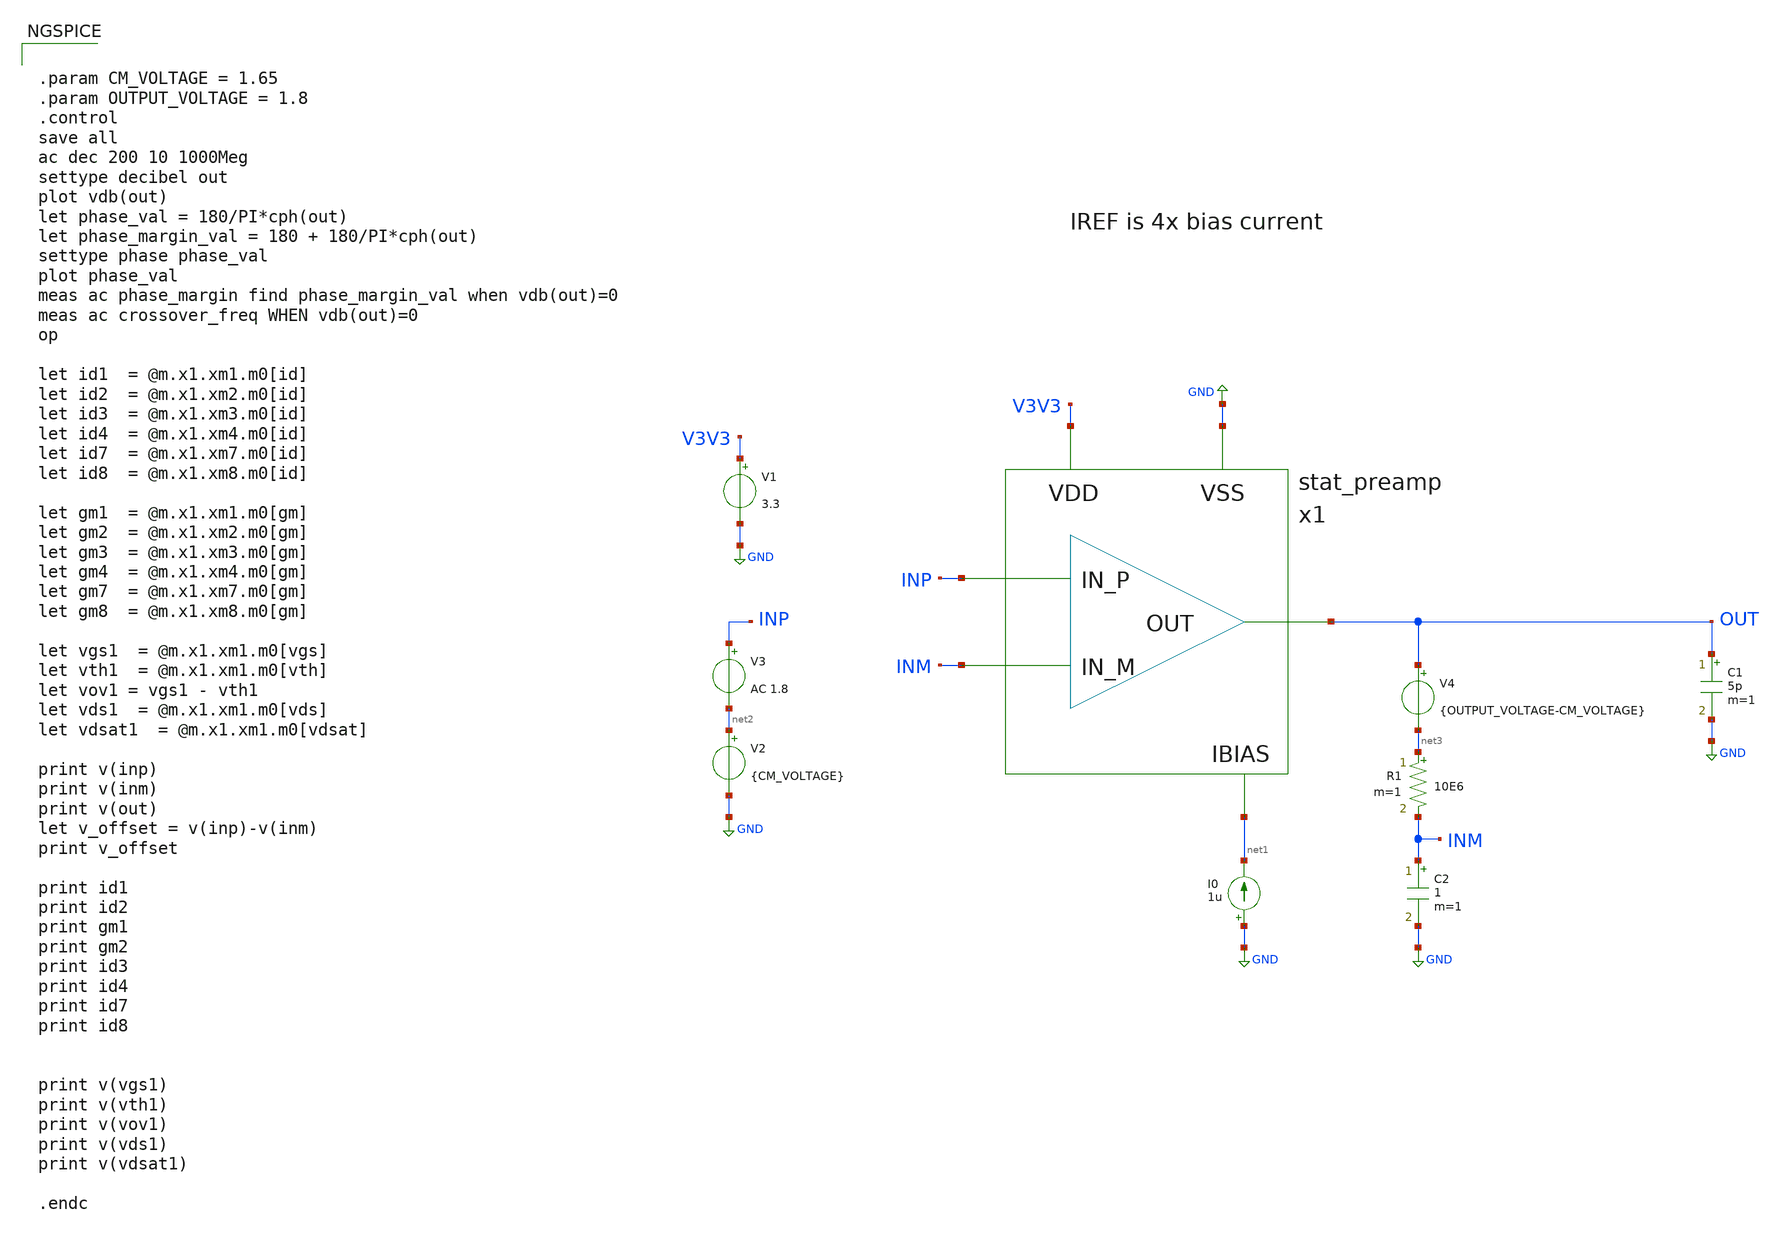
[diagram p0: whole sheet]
** sch_path: SAR_ADC/xschem/test/static_preamp_tb/stat_preamp_tb.sch

.include $env(PDK_ROOT)/$env(PDK)/libs.tech/ngspice/design.ngspice

.lib $env(PDK_ROOT)/$env(PDK)/libs.tech/ngspice/sm141064.ngspice typical
.lib $env(PDK_ROOT)/$env(PDK)/libs.tech/ngspice/sm141064.ngspice mimcap_statistical
.lib $env(PDK_ROOT)/$env(PDK)/libs.tech/ngspice/sm141064.ngspice cap_mim
.lib $env(PDK_ROOT)/$env(PDK)/libs.tech/ngspice/sm141064.ngspice res_typical
.lib $env(PDK_ROOT)/$env(PDK)/libs.tech/ngspice/sm141064.ngspice bjt_typical
.lib $env(PDK_ROOT)/$env(PDK)/libs.tech/ngspice/sm141064.ngspice moscap_typical


**.subckt stat_preamp_tb
V1 V3V3 GND 3.3
I0 GND net1 1u
V2 net2 GND {CM_VOLTAGE}
V3 INP net2 AC 1.8
C1 OUT GND 5p m=1
R1 net3 INM 10E6 m=1
V4 OUT net3 {OUTPUT_VOLTAGE-CM_VOLTAGE}
C2 INM GND 1 m=1
x1 INP INM OUT V3V3 GND net1 stat_preamp
**** begin user architecture code


.param CM_VOLTAGE = 1.65
.param OUTPUT_VOLTAGE = 1.8
.control
save all
ac dec 200 10 1000Meg
settype decibel out
plot vdb(out)
let phase_val = 180/PI*cph(out)
let phase_margin_val = 180 + 180/PI*cph(out)
settype phase phase_val
plot phase_val
meas ac phase_margin find phase_margin_val when vdb(out)=0
meas ac crossover_freq WHEN vdb(out)=0
op

let id1  = @m.x1.xm1.m0[id]
let id2  = @m.x1.xm2.m0[id]
let id3  = @m.x1.xm3.m0[id]
let id4  = @m.x1.xm4.m0[id]
let id7  = @m.x1.xm7.m0[id]
let id8  = @m.x1.xm8.m0[id]

let gm1  = @m.x1.xm1.m0[gm]
let gm2  = @m.x1.xm2.m0[gm]
let gm3  = @m.x1.xm3.m0[gm]
let gm4  = @m.x1.xm4.m0[gm]
let gm7  = @m.x1.xm7.m0[gm]
let gm8  = @m.x1.xm8.m0[gm]

let vgs1  = @m.x1.xm1.m0[vgs]
let vth1  = @m.x1.xm1.m0[vth]
let vov1 = vgs1 - vth1
let vds1  = @m.x1.xm1.m0[vds]
let vdsat1  = @m.x1.xm1.m0[vdsat]

print v(inp)
print v(inm)
print v(out)
let v_offset = v(inp)-v(inm)
print v_offset

print id1
print id2
print gm1
print gm2
print id3
print id4
print id7
print id8


print v(vgs1)
print v(vth1)
print v(vov1)
print v(vds1)
print v(vdsat1)

.endc


**** end user architecture code
**.ends

* expanding   symbol:  ../../../symbols/stat_preamp.sym # of pins=6
** sym_path: SAR_ADC/xschem/designs/stat_preamp.sym
** sch_path: SAR_ADC/xschem/designs/stat_preamp.sch
.subckt stat_preamp IN_P IN_M OUT VDD VSS ibias
*.ipin IN_M
*.ipin IN_P
*.opin OUT
*.iopin VDD
*.iopin VSS
*.iopin ibias
XM3 Vas Vas VDD VDD pfet_03v3 L=3.77u W=5u nf=1 ad='int((nf+1)/2) * W/nf * 0.18u' as='int((nf+2)/2) * W/nf * 0.18u'
+ pd='2*int((nf+1)/2) * (W/nf + 0.18u)' ps='2*int((nf+2)/2) * (W/nf + 0.18u)' nrd='0.18u / W' nrs='0.18u / W'
+ sa=0 sb=0 sd=0 m=1
XM1 Vas IN_M Vsrc VSS nfet_03v3 L=0.3u W=10.59u nf=1 ad='int((nf+1)/2) * W/nf * 0.18u' as='int((nf+2)/2) * W/nf * 0.18u'
+ pd='2*int((nf+1)/2) * (W/nf + 0.18u)' ps='2*int((nf+2)/2) * (W/nf + 0.18u)' nrd='0.18u / W' nrs='0.18u / W'
+ sa=0 sb=0 sd=0 m=1
XM2 OUT IN_P Vsrc VSS nfet_03v3 L=0.3u W=10.59u nf=1 ad='int((nf+1)/2) * W/nf * 0.18u' as='int((nf+2)/2) * W/nf * 0.18u'
+ pd='2*int((nf+1)/2) * (W/nf + 0.18u)' ps='2*int((nf+2)/2) * (W/nf + 0.18u)' nrd='0.18u / W' nrs='0.18u / W'
+ sa=0 sb=0 sd=0 m=1
XM7 Vsrc ibias VSS VSS nfet_03v3 L=4u W=21.8u nf=1 ad='int((nf+1)/2) * W/nf * 0.18u' as='int((nf+2)/2) * W/nf * 0.18u'
+ pd='2*int((nf+1)/2) * (W/nf + 0.18u)' ps='2*int((nf+2)/2) * (W/nf + 0.18u)' nrd='0.18u / W' nrs='0.18u / W'
+ sa=0 sb=0 sd=0 m=1
XM8 ibias ibias VSS VSS nfet_03v3 L=6u W=21.8u nf=1 ad='int((nf+1)/2) * W/nf * 0.18u' as='int((nf+2)/2) * W/nf * 0.18u'
+ pd='2*int((nf+1)/2) * (W/nf + 0.18u)' ps='2*int((nf+2)/2) * (W/nf + 0.18u)' nrd='0.18u / W' nrs='0.18u / W'
+ sa=0 sb=0 sd=0 m=1
XM4 OUT Vas VDD VDD pfet_03v3 L=3.77u W=5u nf=1 ad='int((nf+1)/2) * W/nf * 0.18u' as='int((nf+2)/2) * W/nf * 0.18u'
+ pd='2*int((nf+1)/2) * (W/nf + 0.18u)' ps='2*int((nf+2)/2) * (W/nf + 0.18u)' nrd='0.18u / W' nrs='0.18u / W'
+ sa=0 sb=0 sd=0 m=1
.ends

.GLOBAL GND
.end
